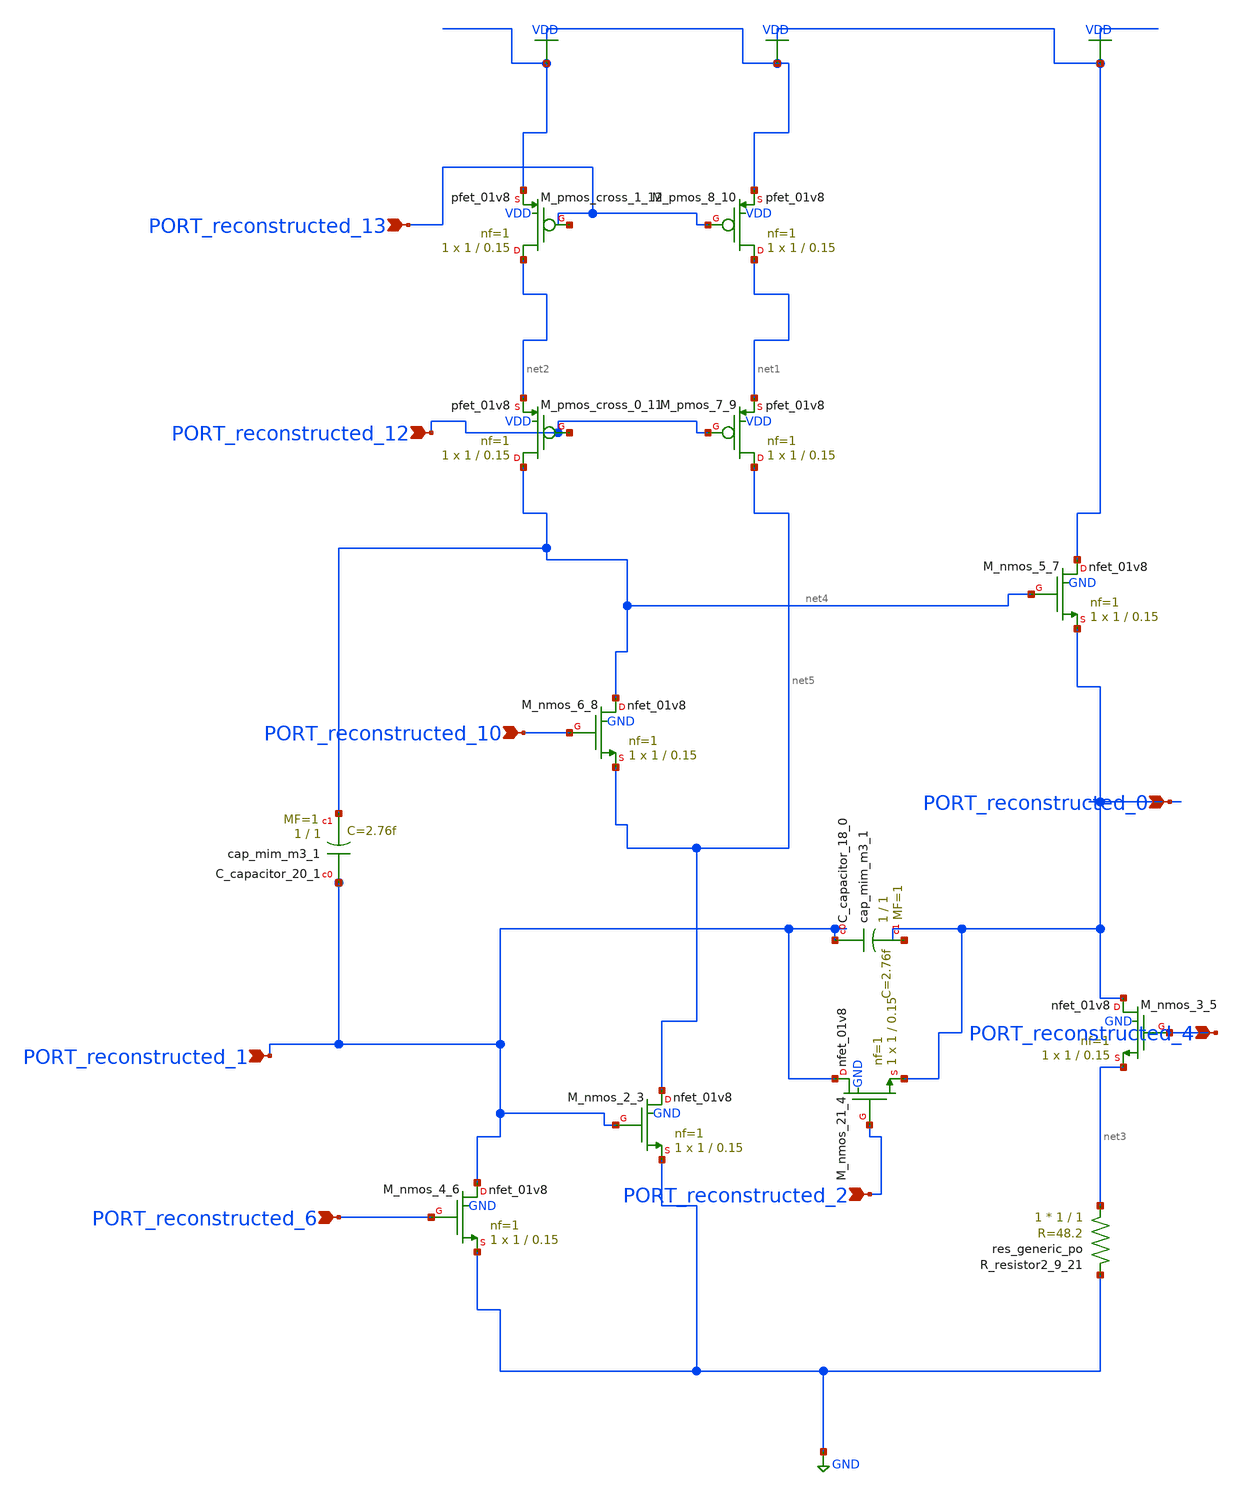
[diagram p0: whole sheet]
** sch_path: schematics/SchemGen/10_1016_j_nima_2022_167570_07_001.sch
**.subckt 10_1016_j_nima_2022_167570_07_001 PORT_reconstructed_13 PORT_reconstructed_2
*+ PORT_reconstructed_12 PORT_reconstructed_1 PORT_reconstructed_10 PORT_reconstructed_6 PORT_reconstructed_4
*+ PORT_reconstructed_0
*.ipin PORT_reconstructed_13
*.ipin PORT_reconstructed_2
*.ipin PORT_reconstructed_12
*.ipin PORT_reconstructed_1
*.ipin PORT_reconstructed_10
*.ipin PORT_reconstructed_6
*.ipin PORT_reconstructed_4
*.ipin PORT_reconstructed_0
XC_capacitor_18_0 PORT_reconstructed_1 PORT_reconstructed_0 sky130_fd_pr__cap_mim_m3_1 W=1 L=1 MF=1
+ m=1
XC_capacitor_20_1 PORT_reconstructed_1 net4 sky130_fd_pr__cap_mim_m3_1 W=1 L=1 MF=1 m=1
XM_nmos_2_3 net5 PORT_reconstructed_1 GND GND sky130_fd_pr__nfet_01v8 L=0.15 W=1 nf=1 ad='int((1 + 1)/2) * 1 / 1 * 0.29'
+ as='int((1 + 2)/2) * 1 / 1 * 0.29' pd='2*int((1 + 1)/2) * (1 / 1 + 0.29)' ps='2*int((1 + 2)/2) * (1 / 1 + 0.29)'
+ nrd='0.29 / 1 ' nrs='0.29 / 1 ' sa=0 sb=0 sd=0 mult=1 m=1
XM_nmos_21_4 PORT_reconstructed_1 PORT_reconstructed_2 PORT_reconstructed_0 GND sky130_fd_pr__nfet_01v8
+ L=0.15 W=1 nf=1 ad='int((1 + 1)/2) * 1 / 1 * 0.29' as='int((1 + 2)/2) * 1 / 1 * 0.29' pd='2*int((1 + 1)/2) * (1 / 1 + 0.29)'
+ ps='2*int((1 + 2)/2) * (1 / 1 + 0.29)' nrd='0.29 / 1 ' nrs='0.29 / 1 ' sa=0 sb=0 sd=0 mult=1 m=1
XM_nmos_3_5 PORT_reconstructed_0 PORT_reconstructed_4 net3 GND sky130_fd_pr__nfet_01v8 L=0.15 W=1 nf=1
+ ad='int((1 + 1)/2) * 1 / 1 * 0.29' as='int((1 + 2)/2) * 1 / 1 * 0.29' pd='2*int((1 + 1)/2) * (1 / 1 + 0.29)'
+ ps='2*int((1 + 2)/2) * (1 / 1 + 0.29)' nrd='0.29 / 1 ' nrs='0.29 / 1 ' sa=0 sb=0 sd=0 mult=1 m=1
XM_nmos_4_6 PORT_reconstructed_1 PORT_reconstructed_6 GND GND sky130_fd_pr__nfet_01v8 L=0.15 W=1 nf=1
+ ad='int((1 + 1)/2) * 1 / 1 * 0.29' as='int((1 + 2)/2) * 1 / 1 * 0.29' pd='2*int((1 + 1)/2) * (1 / 1 + 0.29)'
+ ps='2*int((1 + 2)/2) * (1 / 1 + 0.29)' nrd='0.29 / 1 ' nrs='0.29 / 1 ' sa=0 sb=0 sd=0 mult=1 m=1
XM_nmos_5_7 VDD net4 PORT_reconstructed_0 GND sky130_fd_pr__nfet_01v8 L=0.15 W=1 nf=1 ad='int((1 + 1)/2) * 1 / 1 * 0.29'
+ as='int((1 + 2)/2) * 1 / 1 * 0.29' pd='2*int((1 + 1)/2) * (1 / 1 + 0.29)' ps='2*int((1 + 2)/2) * (1 / 1 + 0.29)'
+ nrd='0.29 / 1 ' nrs='0.29 / 1 ' sa=0 sb=0 sd=0 mult=1 m=1
XM_nmos_6_8 net4 PORT_reconstructed_10 net5 GND sky130_fd_pr__nfet_01v8 L=0.15 W=1 nf=1 ad='int((1 + 1)/2) * 1 / 1 * 0.29'
+ as='int((1 + 2)/2) * 1 / 1 * 0.29' pd='2*int((1 + 1)/2) * (1 / 1 + 0.29)' ps='2*int((1 + 2)/2) * (1 / 1 + 0.29)'
+ nrd='0.29 / 1 ' nrs='0.29 / 1 ' sa=0 sb=0 sd=0 mult=1 m=1
XM_pmos_7_9 net5 PORT_reconstructed_12 net1 VDD sky130_fd_pr__pfet_01v8 L=0.15 W=1 nf=1 ad='int((1 + 1)/2) * 1 / 1 * 0.29'
+ as='int((1 + 2)/2) * 1 / 1 * 0.29' pd='2*int((1 + 1)/2) * (1 / 1 + 0.29)' ps='2*int((1 + 2)/2) * (1 / 1 + 0.29)'
+ nrd='0.29 / 1 ' nrs='0.29 / 1 ' sa=0 sb=0 sd=0 mult=1 m=1
XM_pmos_8_10 net1 PORT_reconstructed_13 VDD VDD sky130_fd_pr__pfet_01v8 L=0.15 W=1 nf=1 ad='int((1 + 1)/2) * 1 / 1 * 0.29'
+ as='int((1 + 2)/2) * 1 / 1 * 0.29' pd='2*int((1 + 1)/2) * (1 / 1 + 0.29)' ps='2*int((1 + 2)/2) * (1 / 1 + 0.29)'
+ nrd='0.29 / 1 ' nrs='0.29 / 1 ' sa=0 sb=0 sd=0 mult=1 m=1
XM_pmos_cross_0_11 net4 PORT_reconstructed_12 net2 VDD sky130_fd_pr__pfet_01v8 L=0.15 W=1 nf=1 ad='int((1 + 1)/2) * 1 / 1 * 0.29'
+ as='int((1 + 2)/2) * 1 / 1 * 0.29' pd='2*int((1 + 1)/2) * (1 / 1 + 0.29)' ps='2*int((1 + 2)/2) * (1 / 1 + 0.29)'
+ nrd='0.29 / 1 ' nrs='0.29 / 1 ' sa=0 sb=0 sd=0 mult=1 m=1
XM_pmos_cross_1_12 net2 PORT_reconstructed_13 VDD VDD sky130_fd_pr__pfet_01v8 L=0.15 W=1 nf=1 ad='int((1 + 1)/2) * 1 / 1 * 0.29'
+ as='int((1 + 2)/2) * 1 / 1 * 0.29' pd='2*int((1 + 1)/2) * (1 / 1 + 0.29)' ps='2*int((1 + 2)/2) * (1 / 1 + 0.29)'
+ nrd='0.29 / 1 ' nrs='0.29 / 1 ' sa=0 sb=0 sd=0 mult=1 m=1
XR_resistor2_9_21 net3 GND sky130_fd_pr__res_generic_po W=1 L=1 m=1
**.ends
.GLOBAL GND
.GLOBAL VDD
.end
